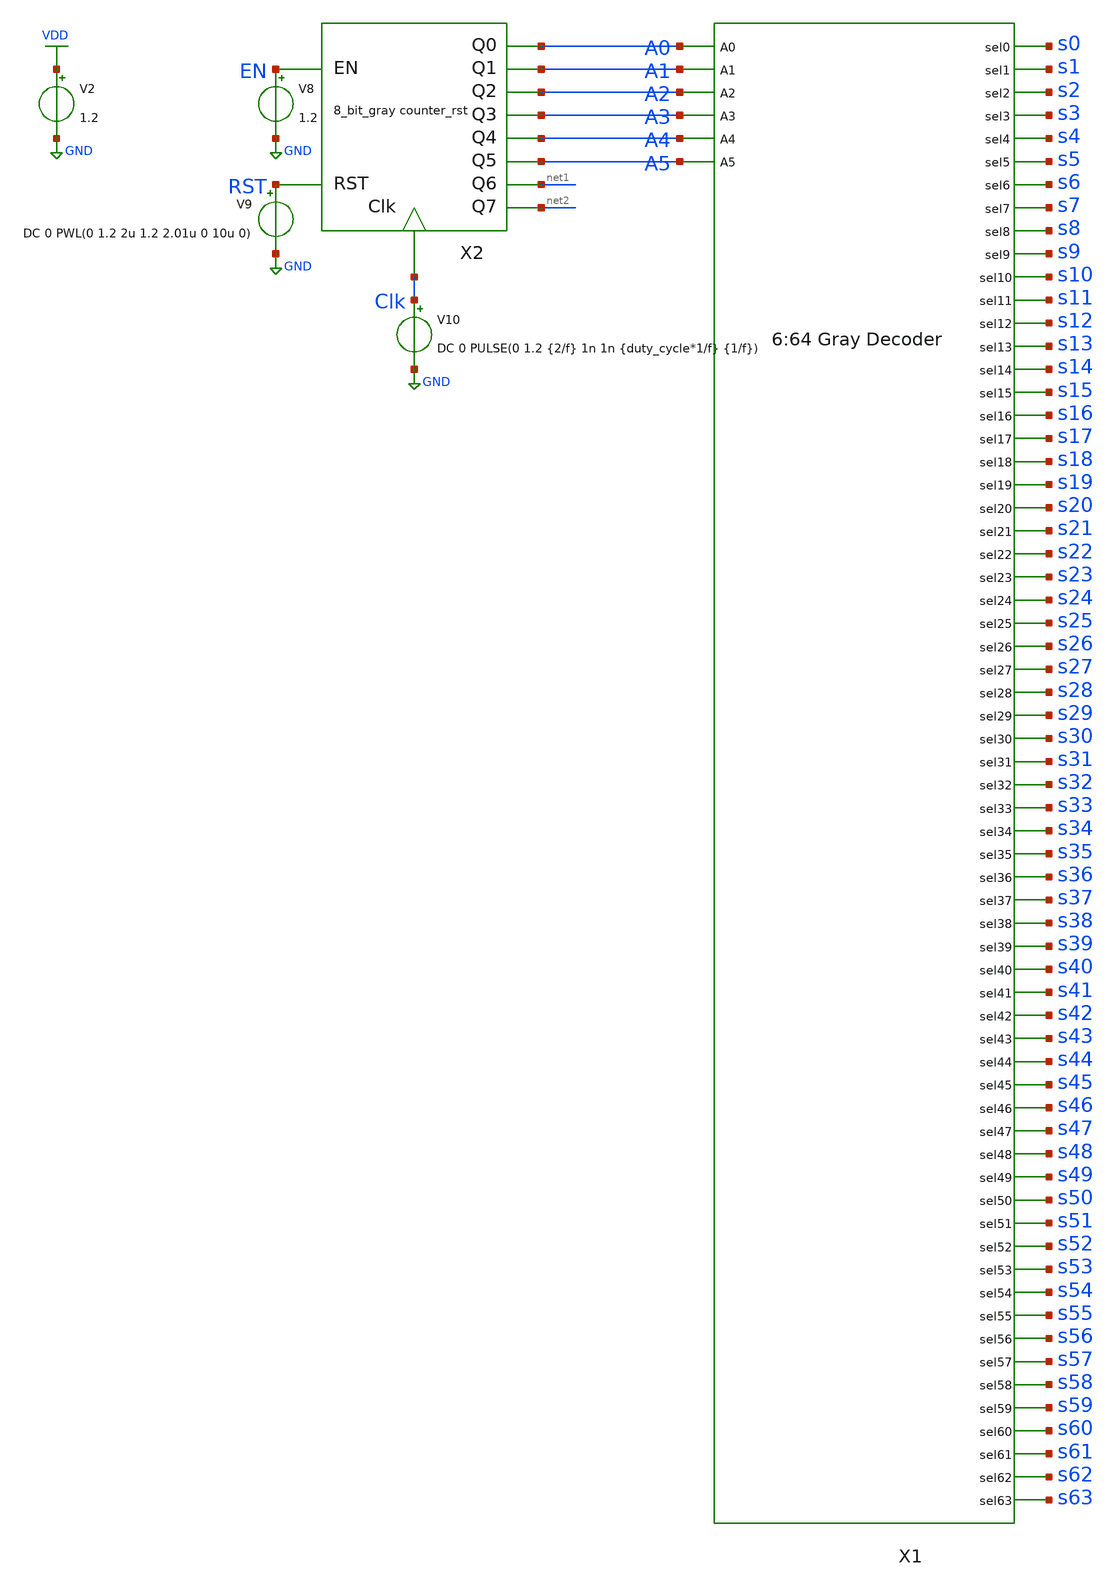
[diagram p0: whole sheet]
** sch_path: xschem/decoder/6_64_gray_decoder_tb.sch
**.subckt 6_64_gray_decoder_tb
X1 A0 A1 A2 A3 A4 A5 s0 s1 s2 s3 s4 s5 s6 s7 s8 s9 s10 s11 s12 s13 s14 s15 s16 s17 s18 s19 s20 s21
+ s22 s23 s24 s25 s26 s27 s28 s29 s30 s31 s32 s33 s34 s35 s36 s37 s38 s39 s40 s41 s42 s43 s44 s45 s46 s47
+ s48 s49 s50 s51 s52 s53 s54 s55 s56 s57 s58 s59 s60 s61 s62 s63 6_64_gray_decoder
V2 VDD GND 1.2
X2 EN A1 net1 Clk A0 A2 A3 A4 A5 net2 RST 8_bit_gray_counter_rst
V8 EN GND 1.2
V9 RST GND DC 0 PWL(0 1.2 2u 1.2 2.01u 0 10u 0)
V10 Clk GND DC 0 PULSE(0 1.2 {2/f} 1n 1n {duty_cycle*1/f} {1/f})
**** begin user architecture code


.lib /home/sky/sky130A/libs.tech/ngspice/sky130.lib.spice tt
.include /home/sky/sky130A/libs.ref/sky130_fd_sc_lp/spice/sky130_fd_sc_lp.spice
.options abstol=1e-14 reltol=1e-4
.param f=80k
.param duty_cycle=0.5
*.ic v(Q)=0 v(Q_inv)=1 v(x1.net1)=0
.tran {(1/100)*(1/f)} {40/f}
.save all


**** end user architecture code
**.ends
.GLOBAL GND
.GLOBAL VDD
.end
